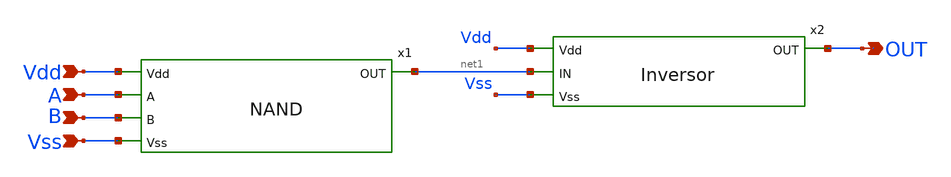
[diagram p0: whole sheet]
** sch_path: icdesign/sch/And/AND.sch
**.subckt AND Vss Vdd A OUT B
*.ipin Vss
*.ipin Vdd
*.ipin A
*.opin OUT
*.ipin B
x1 Vdd A B net1 Vss NAND
x2 Vdd net1 OUT Vss Inversor
**.ends

* expanding   symbol:  NAND/NAND.sym # of pins=5
** sym_path: icdesign/sch/NAND/NAND.sym
** sch_path: icdesign/sch/NAND/NAND.sch
.subckt NAND Vdd A B OUT Vss
*.ipin A
*.ipin B
*.ipin Vdd
*.ipin Vss
*.opin OUT
XM1 net1 B Vss Vss sky130_fd_pr__nfet_01v8 L=0.15 W=0.75 nf=1 ad='int((nf+1)/2) * W/nf * 0.29' as='int((nf+2)/2) * W/nf * 0.29'
+ pd='2*int((nf+1)/2) * (W/nf + 0.29)' ps='2*int((nf+2)/2) * (W/nf + 0.29)' nrd='0.29 / W' nrs='0.29 / W'
+ sa=0 sb=0 sd=0 mult=2 m=2
XM2 OUT A net1 Vss sky130_fd_pr__nfet_01v8 L=0.15 W=0.75 nf=1 ad='int((nf+1)/2) * W/nf * 0.29' as='int((nf+2)/2) * W/nf * 0.29'
+ pd='2*int((nf+1)/2) * (W/nf + 0.29)' ps='2*int((nf+2)/2) * (W/nf + 0.29)' nrd='0.29 / W' nrs='0.29 / W'
+ sa=0 sb=0 sd=0 mult=2 m=2
XM5 OUT B Vdd Vdd sky130_fd_pr__pfet_01v8 L=0.15 W=0.75 nf=1 ad='int((nf+1)/2) * W/nf * 0.29' as='int((nf+2)/2) * W/nf * 0.29'
+ pd='2*int((nf+1)/2) * (W/nf + 0.29)' ps='2*int((nf+2)/2) * (W/nf + 0.29)' nrd='0.29 / W' nrs='0.29 / W'
+ sa=0 sb=0 sd=0 mult=2 m=2
XM4 OUT A Vdd Vdd sky130_fd_pr__pfet_01v8 L=0.15 W=0.75 nf=1 ad='int((nf+1)/2) * W/nf * 0.29' as='int((nf+2)/2) * W/nf * 0.29'
+ pd='2*int((nf+1)/2) * (W/nf + 0.29)' ps='2*int((nf+2)/2) * (W/nf + 0.29)' nrd='0.29 / W' nrs='0.29 / W'
+ sa=0 sb=0 sd=0 mult=2 m=2
.ends


* expanding   symbol:  Inversor/Inversor.sym # of pins=4
** sym_path: icdesign/sch/Inversor/Inversor.sym
** sch_path: icdesign/sch/Inversor/Inversor.sch
.subckt Inversor Vdd IN OUT Vss
*.ipin IN
*.ipin Vdd
*.ipin Vss
*.opin OUT
XM1 OUT IN Vss Vss sky130_fd_pr__nfet_01v8 L=0.15 W=0.75 nf=1 ad='int((nf+1)/2) * W/nf * 0.29' as='int((nf+2)/2) * W/nf * 0.29'
+ pd='2*int((nf+1)/2) * (W/nf + 0.29)' ps='2*int((nf+2)/2) * (W/nf + 0.29)' nrd='0.29 / W' nrs='0.29 / W'
+ sa=0 sb=0 sd=0 mult=1 m=1
XM2 OUT IN Vdd Vdd sky130_fd_pr__pfet_01v8 L=0.15 W=0.75 nf=1 ad='int((nf+1)/2) * W/nf * 0.29' as='int((nf+2)/2) * W/nf * 0.29'
+ pd='2*int((nf+1)/2) * (W/nf + 0.29)' ps='2*int((nf+2)/2) * (W/nf + 0.29)' nrd='0.29 / W' nrs='0.29 / W'
+ sa=0 sb=0 sd=0 mult=2 m=2
.ends

.end
